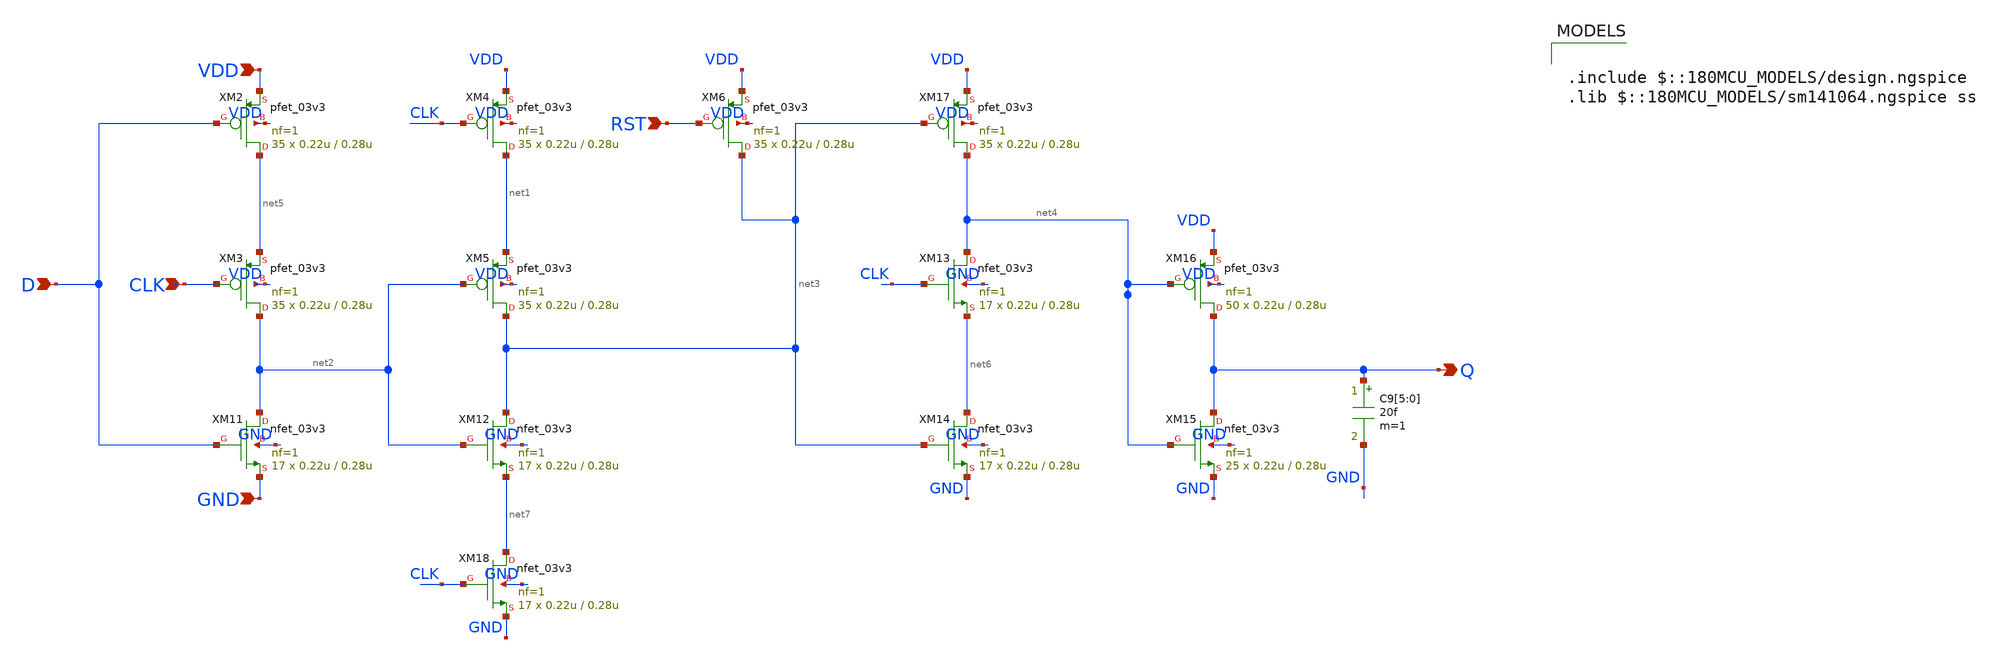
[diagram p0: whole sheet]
** sch_path: blocks/adc/encoder/tb/dff_test.sch
**.subckt dff_test Q D CLK RST VDD GND
*.opin Q
*.ipin D
*.ipin CLK
*.ipin RST
*.ipin VDD
*.ipin GND
XM2 net5 D VDD VDD pfet_03v3 L=0.28u W=0.22u nf=1 ad='int((nf+1)/2) * W/nf * 0.18u' as='int((nf+2)/2) * W/nf * 0.18u'
+ pd='2*int((nf+1)/2) * (W/nf + 0.18u)' ps='2*int((nf+2)/2) * (W/nf + 0.18u)' nrd='0.18u / W' nrs='0.18u / W'
+ sa=0 sb=0 sd=0 m=35
XM3 net2 CLK net5 VDD pfet_03v3 L=0.28u W=0.22u nf=1 ad='int((nf+1)/2) * W/nf * 0.18u' as='int((nf+2)/2) * W/nf * 0.18u'
+ pd='2*int((nf+1)/2) * (W/nf + 0.18u)' ps='2*int((nf+2)/2) * (W/nf + 0.18u)' nrd='0.18u / W' nrs='0.18u / W'
+ sa=0 sb=0 sd=0 m=35
XM4 net1 CLK VDD VDD pfet_03v3 L=0.28u W=0.22u nf=1 ad='int((nf+1)/2) * W/nf * 0.18u' as='int((nf+2)/2) * W/nf * 0.18u'
+ pd='2*int((nf+1)/2) * (W/nf + 0.18u)' ps='2*int((nf+2)/2) * (W/nf + 0.18u)' nrd='0.18u / W' nrs='0.18u / W'
+ sa=0 sb=0 sd=0 m=35
XM5 net3 net2 net1 VDD pfet_03v3 L=0.28u W=0.22u nf=1 ad='int((nf+1)/2) * W/nf * 0.18u' as='int((nf+2)/2) * W/nf * 0.18u'
+ pd='2*int((nf+1)/2) * (W/nf + 0.18u)' ps='2*int((nf+2)/2) * (W/nf + 0.18u)' nrd='0.18u / W' nrs='0.18u / W'
+ sa=0 sb=0 sd=0 m=35
XM6 net3 RST VDD VDD pfet_03v3 L=0.28u W=0.22u nf=1 ad='int((nf+1)/2) * W/nf * 0.18u' as='int((nf+2)/2) * W/nf * 0.18u'
+ pd='2*int((nf+1)/2) * (W/nf + 0.18u)' ps='2*int((nf+2)/2) * (W/nf + 0.18u)' nrd='0.18u / W' nrs='0.18u / W'
+ sa=0 sb=0 sd=0 m=35
XM11 net2 D GND GND nfet_03v3 L=0.28u W=0.22u nf=1 ad='int((nf+1)/2) * W/nf * 0.18u' as='int((nf+2)/2) * W/nf * 0.18u'
+ pd='2*int((nf+1)/2) * (W/nf + 0.18u)' ps='2*int((nf+2)/2) * (W/nf + 0.18u)' nrd='0.18u / W' nrs='0.18u / W'
+ sa=0 sb=0 sd=0 m=17
XM12 net3 net2 net7 GND nfet_03v3 L=0.28u W=0.22u nf=1 ad='int((nf+1)/2) * W/nf * 0.18u' as='int((nf+2)/2) * W/nf * 0.18u'
+ pd='2*int((nf+1)/2) * (W/nf + 0.18u)' ps='2*int((nf+2)/2) * (W/nf + 0.18u)' nrd='0.18u / W' nrs='0.18u / W'
+ sa=0 sb=0 sd=0 m=17
XM13 net4 CLK net6 GND nfet_03v3 L=0.28u W=0.22u nf=1 ad='int((nf+1)/2) * W/nf * 0.18u' as='int((nf+2)/2) * W/nf * 0.18u'
+ pd='2*int((nf+1)/2) * (W/nf + 0.18u)' ps='2*int((nf+2)/2) * (W/nf + 0.18u)' nrd='0.18u / W' nrs='0.18u / W'
+ sa=0 sb=0 sd=0 m=17
XM14 net6 net3 GND GND nfet_03v3 L=0.28u W=0.22u nf=1 ad='int((nf+1)/2) * W/nf * 0.18u' as='int((nf+2)/2) * W/nf * 0.18u'
+ pd='2*int((nf+1)/2) * (W/nf + 0.18u)' ps='2*int((nf+2)/2) * (W/nf + 0.18u)' nrd='0.18u / W' nrs='0.18u / W'
+ sa=0 sb=0 sd=0 m=17
XM15 Q net4 GND GND nfet_03v3 L=0.28u W=0.22u nf=1 ad='int((nf+1)/2) * W/nf * 0.18u' as='int((nf+2)/2) * W/nf * 0.18u'
+ pd='2*int((nf+1)/2) * (W/nf + 0.18u)' ps='2*int((nf+2)/2) * (W/nf + 0.18u)' nrd='0.18u / W' nrs='0.18u / W'
+ sa=0 sb=0 sd=0 m=25
XM16 Q net4 VDD VDD pfet_03v3 L=0.28u W=0.22u nf=1 ad='int((nf+1)/2) * W/nf * 0.18u' as='int((nf+2)/2) * W/nf * 0.18u'
+ pd='2*int((nf+1)/2) * (W/nf + 0.18u)' ps='2*int((nf+2)/2) * (W/nf + 0.18u)' nrd='0.18u / W' nrs='0.18u / W'
+ sa=0 sb=0 sd=0 m=50
XM17 net4 net3 VDD VDD pfet_03v3 L=0.28u W=0.22u nf=1 ad='int((nf+1)/2) * W/nf * 0.18u' as='int((nf+2)/2) * W/nf * 0.18u'
+ pd='2*int((nf+1)/2) * (W/nf + 0.18u)' ps='2*int((nf+2)/2) * (W/nf + 0.18u)' nrd='0.18u / W' nrs='0.18u / W'
+ sa=0 sb=0 sd=0 m=35
XM18 net7 CLK GND GND nfet_03v3 L=0.28u W=0.22u nf=1 ad='int((nf+1)/2) * W/nf * 0.18u' as='int((nf+2)/2) * W/nf * 0.18u'
+ pd='2*int((nf+1)/2) * (W/nf + 0.18u)' ps='2*int((nf+2)/2) * (W/nf + 0.18u)' nrd='0.18u / W' nrs='0.18u / W'
+ sa=0 sb=0 sd=0 m=17
C9[5] Q GND 20f m=1
C9[4] Q GND 20f m=1
C9[3] Q GND 20f m=1
C9[2] Q GND 20f m=1
C9[1] Q GND 20f m=1
C9[0] Q GND 20f m=1
**** begin user architecture code

.include $::180MCU_MODELS/design.ngspice
.lib $::180MCU_MODELS/sm141064.ngspice ss



V_VDD VDD 0 3.3

V_CLK CLK 0 pulse(0 3.3 260p 10p 10p 290p 500p)
V_D D 0 pwl(0 0 250p 0 260p 3.3 300p 3.3 310p 0 1.75n 0)
V_RST RST 0 pulse(3.3 3.3 0s 10p 10p 240p 500p)
.control
  save CLK D RST Q
  run
  write tspc_dff_rst_test.raw
.endc
.tran 1p 5n



**** end user architecture code
**.ends
.end
